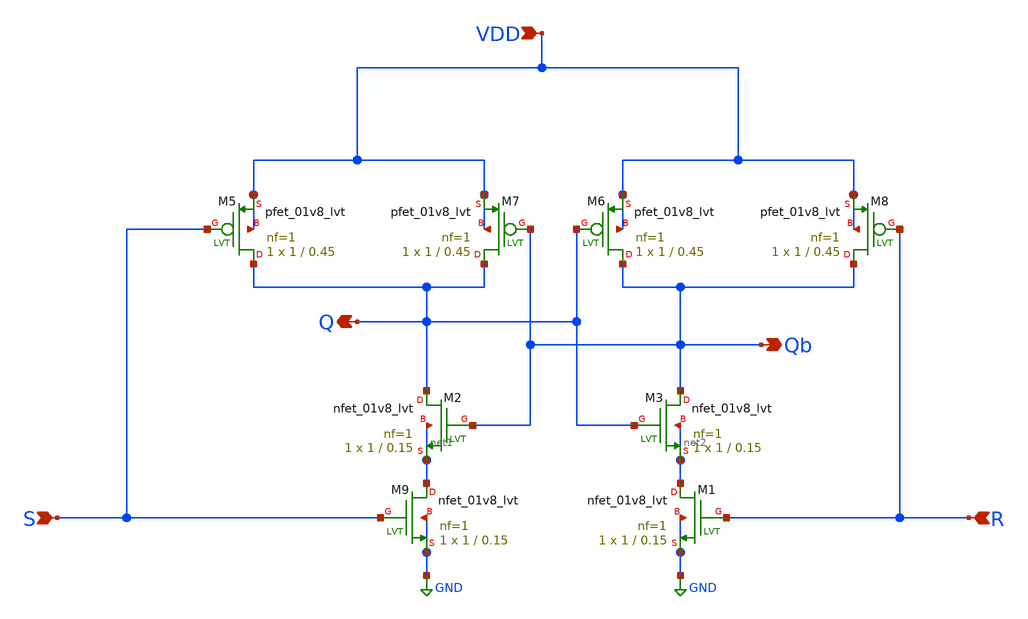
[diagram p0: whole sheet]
** sch_path: Current Sensor/sr_latch.sch
**.subckt sr_latch S R Qb Q VDD
*.ipin S
*.ipin R
*.opin Qb
*.opin Q
*.ipin VDD
XM9 net1 S GND GND sky130_fd_pr__nfet_01v8_lvt L=0.15 W=1 nf=1 ad='int((nf+1)/2) * W/nf * 0.29' as='int((nf+2)/2) * W/nf * 0.29'
+ pd='2*int((nf+1)/2) * (W/nf + 0.29)' ps='2*int((nf+2)/2) * (W/nf + 0.29)' nrd='0.29 / W' nrs='0.29 / W'
+ sa=0 sb=0 sd=0 mult=1 m=1
XM1 net2 R GND GND sky130_fd_pr__nfet_01v8_lvt L=0.15 W=1 nf=1 ad='int((nf+1)/2) * W/nf * 0.29' as='int((nf+2)/2) * W/nf * 0.29'
+ pd='2*int((nf+1)/2) * (W/nf + 0.29)' ps='2*int((nf+2)/2) * (W/nf + 0.29)' nrd='0.29 / W' nrs='0.29 / W'
+ sa=0 sb=0 sd=0 mult=1 m=1
XM2 Q Qb net1 net1 sky130_fd_pr__nfet_01v8_lvt L=0.15 W=1 nf=1 ad='int((nf+1)/2) * W/nf * 0.29' as='int((nf+2)/2) * W/nf * 0.29'
+ pd='2*int((nf+1)/2) * (W/nf + 0.29)' ps='2*int((nf+2)/2) * (W/nf + 0.29)' nrd='0.29 / W' nrs='0.29 / W'
+ sa=0 sb=0 sd=0 mult=1 m=1
XM3 Qb Q net2 net2 sky130_fd_pr__nfet_01v8_lvt L=0.15 W=1 nf=1 ad='int((nf+1)/2) * W/nf * 0.29' as='int((nf+2)/2) * W/nf * 0.29'
+ pd='2*int((nf+1)/2) * (W/nf + 0.29)' ps='2*int((nf+2)/2) * (W/nf + 0.29)' nrd='0.29 / W' nrs='0.29 / W'
+ sa=0 sb=0 sd=0 mult=1 m=1
XM5 Q S VDD VDD sky130_fd_pr__pfet_01v8_lvt L=0.45 W=1 nf=1 ad='int((nf+1)/2) * W/nf * 0.29' as='int((nf+2)/2) * W/nf * 0.29'
+ pd='2*int((nf+1)/2) * (W/nf + 0.29)' ps='2*int((nf+2)/2) * (W/nf + 0.29)' nrd='0.29 / W' nrs='0.29 / W'
+ sa=0 sb=0 sd=0 mult=1 m=1
XM6 Qb Q VDD VDD sky130_fd_pr__pfet_01v8_lvt L=0.45 W=1 nf=1 ad='int((nf+1)/2) * W/nf * 0.29' as='int((nf+2)/2) * W/nf * 0.29'
+ pd='2*int((nf+1)/2) * (W/nf + 0.29)' ps='2*int((nf+2)/2) * (W/nf + 0.29)' nrd='0.29 / W' nrs='0.29 / W'
+ sa=0 sb=0 sd=0 mult=1 m=1
XM7 Q Qb VDD VDD sky130_fd_pr__pfet_01v8_lvt L=0.45 W=1 nf=1 ad='int((nf+1)/2) * W/nf * 0.29' as='int((nf+2)/2) * W/nf * 0.29'
+ pd='2*int((nf+1)/2) * (W/nf + 0.29)' ps='2*int((nf+2)/2) * (W/nf + 0.29)' nrd='0.29 / W' nrs='0.29 / W'
+ sa=0 sb=0 sd=0 mult=1 m=1
XM8 Qb R VDD VDD sky130_fd_pr__pfet_01v8_lvt L=0.45 W=1 nf=1 ad='int((nf+1)/2) * W/nf * 0.29' as='int((nf+2)/2) * W/nf * 0.29'
+ pd='2*int((nf+1)/2) * (W/nf + 0.29)' ps='2*int((nf+2)/2) * (W/nf + 0.29)' nrd='0.29 / W' nrs='0.29 / W'
+ sa=0 sb=0 sd=0 mult=1 m=1
**.ends
.GLOBAL GND
.end
